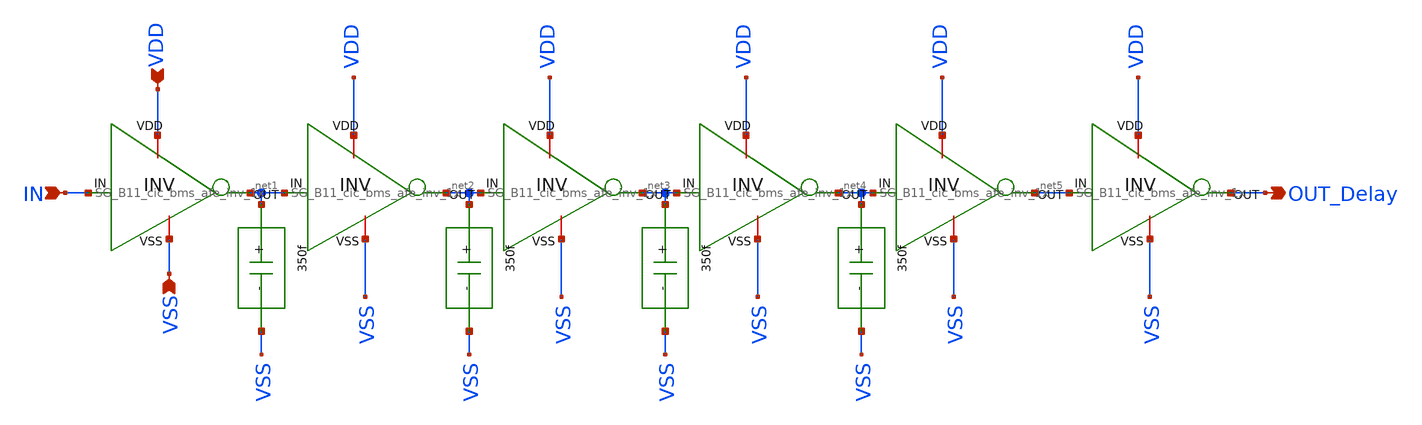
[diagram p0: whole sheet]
** sch_path: design/schematics/EIS/NOCG/SG_B11_cic_bms_afe_delay_block_5V.sch
**.subckt SG_B11_cic_bms_afe_delay_block_5V VDD VSS OUT_Delay IN
*.ipin VDD
*.ipin VSS
*.opin OUT_Delay
*.ipin IN
x1 VDD net1 IN VSS SG_B11_cic_bms_afe_inv_1x
x2 VDD net2 net1 VSS SG_B11_cic_bms_afe_inv_1x
x4 VDD net4 net3 VSS SG_B11_cic_bms_afe_inv_1x
x5 VDD net5 net4 VSS SG_B11_cic_bms_afe_inv_1x
x6 VDD OUT_Delay net5 VSS SG_B11_cic_bms_afe_inv_1x
x7 net1 VSS SG_B11_cic_bms_afe_delay_cap
x8 net2 VSS SG_B11_cic_bms_afe_delay_cap
x9 net3 VSS SG_B11_cic_bms_afe_delay_cap
x10 net4 VSS SG_B11_cic_bms_afe_delay_cap
x3 VDD net3 net2 VSS SG_B11_cic_bms_afe_inv_1x
**.ends
.end
